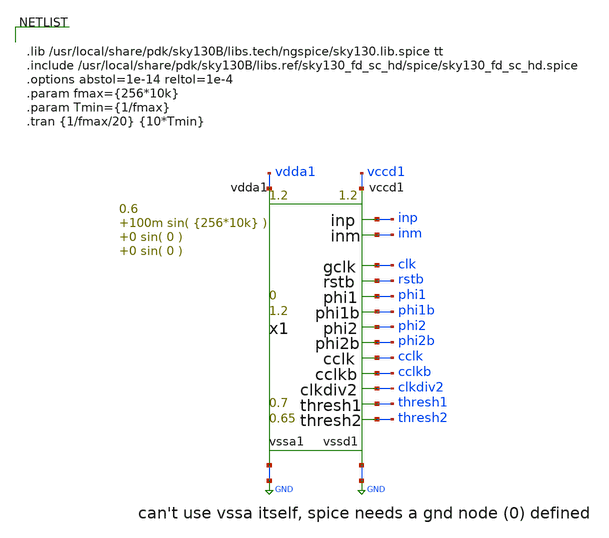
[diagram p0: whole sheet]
** sch_path: xschem/risc_signals_tb.sch
**.subckt risc_signals_tb
x1 thresh1 thresh2 vdda1 GND inp inm clk rstb vccd1 GND phi1 phi1b phi2 phi2b cclk cclkb clkdiv2 risc_signals
+ p_vdda1=1.2 p_vccd1=1.2 p_fclk={256*10k} p_duty_cycle=0.5 p_rstb_delay={1.5/p_fclk} p_rstb_tr=5n p_thresh1=0.7
+ p_thresh2=0.65 p_vpb=0 p_vnb=1.2 p_vcm=0.6 p_amp1=100m p_f1={256*10k} p_amp2=0 p_f2=0 p_amp3=0 p_f3=0
**** begin user architecture code


.lib /usr/local/share/pdk/sky130B/libs.tech/ngspice/sky130.lib.spice tt
.include /usr/local/share/pdk/sky130B/libs.ref/sky130_fd_sc_hd/spice/sky130_fd_sc_hd.spice
.options abstol=1e-14 reltol=1e-4
.param fmax={256*10k}
.param Tmin={1/fmax}
.tran {1/fmax/20} {10*Tmin}


**** end user architecture code
**.ends
.GLOBAL GND
.end
